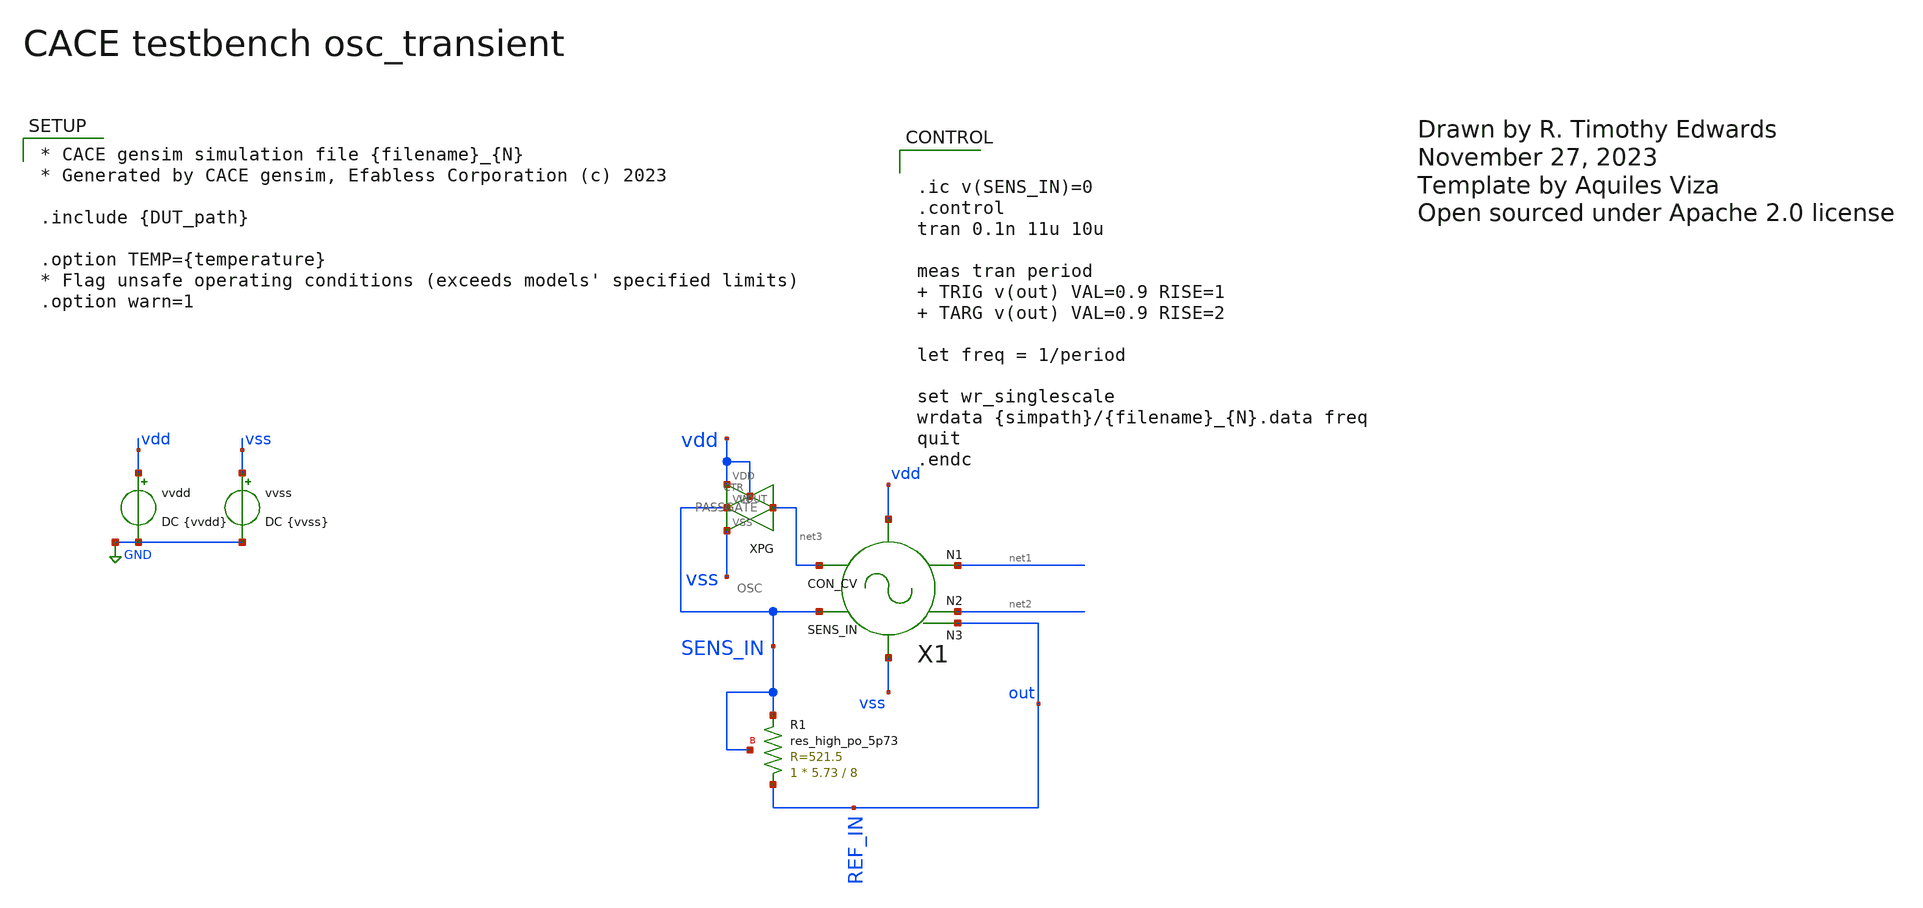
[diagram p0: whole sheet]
** sch_path: modules/cace/osc_transient.sch
* Open sourced under Apache 2.0 license

* CACE gensim simulation file {filename}_{N}
* Generated by CACE gensim, Efabless Corporation (c) 2023

.include {DUT_path}

.option TEMP={temperature}
* Flag unsafe operating conditions (exceeds models' specified limits)
.option warn=1


**.subckt osc_transient
vvss vss GND DC {vvss}
vvdd vdd GND DC {vvdd}
X1 SENS_IN net1 net2 vdd vss net3 out OSC
XR1 out SENS_IN SENS_IN sky130_fd_pr__res_high_po_5p73 L=8 mult=1 m=1
XPG SENS_IN vdd net3 vdd vss PASSGATE
**** begin user architecture code


.ic v(SENS_IN)=0
.control
tran 0.1n 11u 10u

meas tran period  TRIG v(out) VAL=0.9 RISE=1  TARG v(out) VAL=0.9 RISE=2

let freq = 1/period

set wr_singlescale
wrdata {simpath}/{filename}_{N}.data freq
quit
.endc



.lib $env(PDK_ROOT)/$env(PDK)/libs.tech/ngspice/sky130.lib.spice.tt.red {corner}

.include $env(PDK_ROOT)/$env(PDK)/libs.ref/sky130_fd_sc_hd/spice/sky130_fd_sc_hd.spice

**** end user architecture code
**.ends
.GLOBAL GND
.end
